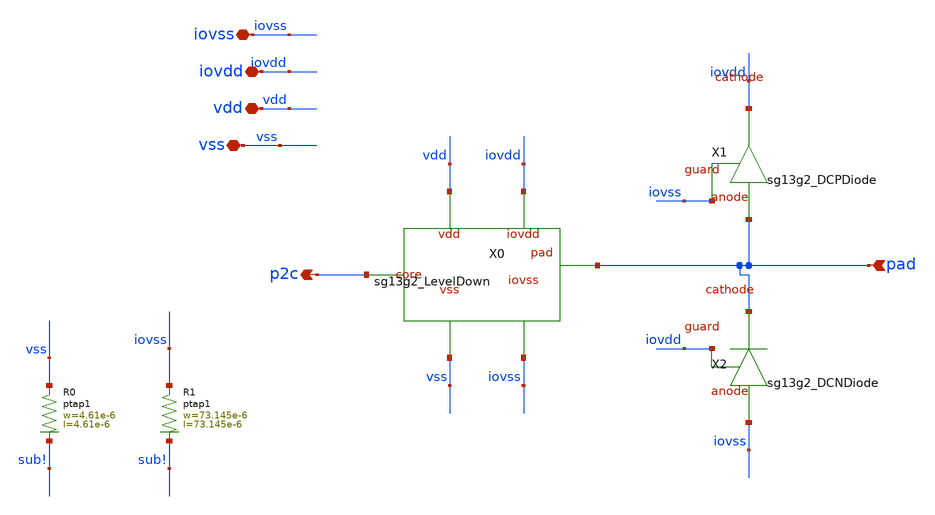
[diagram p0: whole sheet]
** sch_path: ihp-sg13g2/libs.ref/sg13g2_io/sch/xschem/sg13g2_IOPadIn.sch
**.subckt sg13g2_IOPadIn vdd vss iovdd pad iovss p2c
*.iopin vdd
*.iopin vss
*.iopin iovdd
*.ipin pad
*.iopin iovss
*.opin p2c
X0 p2c vss vdd pad iovss iovdd sg13g2_LevelDown
X1 iovss iovdd pad sg13g2_DCPDiode
X2 iovdd pad iovss sg13g2_DCNDiode
XR0 vss sub! ptap1 R=24.69 w=4.61e-6 l=4.61e-6
XR1 iovss sub! ptap1 R=173.7m w=73.145e-6 l=73.145e-6
**.ends
.end
